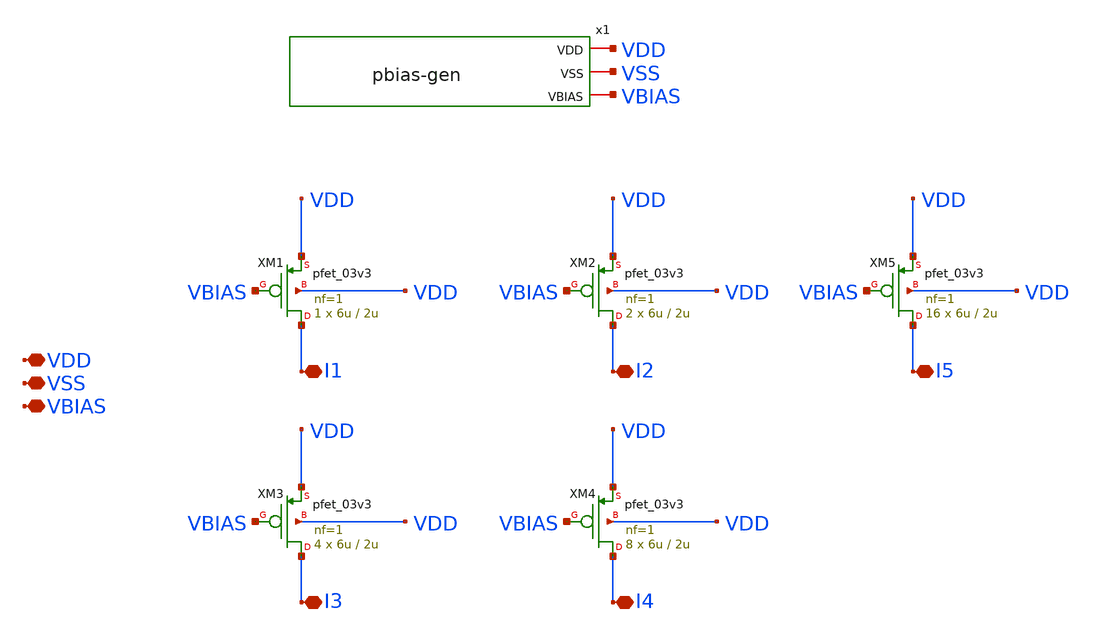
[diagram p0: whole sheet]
** sch_path: designs/libs/OTA/pmos_current_mirror-lna.sch
**.subckt pmos_current_mirror-lna VDD VSS VBIAS I1 I2 I3 I4 I5
*.iopin VDD
*.iopin VSS
*.iopin VBIAS
*.iopin I1
*.iopin I2
*.iopin I3
*.iopin I4
*.iopin I5
x1 VDD VSS VBIAS pbias-gen
XM1 I1 VBIAS VDD VDD pfet_03v3 L=2u W=6u nf=1 ad='int((nf+1)/2) * W/nf * 0.18u' as='int((nf+2)/2) * W/nf * 0.18u'
+ pd='2*int((nf+1)/2) * (W/nf + 0.18u)' ps='2*int((nf+2)/2) * (W/nf + 0.18u)' nrd='0.18u / W' nrs='0.18u / W'
+ sa=0 sb=0 sd=0 m=1
XM2 I2 VBIAS VDD VDD pfet_03v3 L=2u W=6u nf=1 ad='int((nf+1)/2) * W/nf * 0.18u' as='int((nf+2)/2) * W/nf * 0.18u'
+ pd='2*int((nf+1)/2) * (W/nf + 0.18u)' ps='2*int((nf+2)/2) * (W/nf + 0.18u)' nrd='0.18u / W' nrs='0.18u / W'
+ sa=0 sb=0 sd=0 m=2
XM3 I3 VBIAS VDD VDD pfet_03v3 L=2u W=6u nf=1 ad='int((nf+1)/2) * W/nf * 0.18u' as='int((nf+2)/2) * W/nf * 0.18u'
+ pd='2*int((nf+1)/2) * (W/nf + 0.18u)' ps='2*int((nf+2)/2) * (W/nf + 0.18u)' nrd='0.18u / W' nrs='0.18u / W'
+ sa=0 sb=0 sd=0 m=4
XM4 I4 VBIAS VDD VDD pfet_03v3 L=2u W=6u nf=1 ad='int((nf+1)/2) * W/nf * 0.18u' as='int((nf+2)/2) * W/nf * 0.18u'
+ pd='2*int((nf+1)/2) * (W/nf + 0.18u)' ps='2*int((nf+2)/2) * (W/nf + 0.18u)' nrd='0.18u / W' nrs='0.18u / W'
+ sa=0 sb=0 sd=0 m=8
XM5 I5 VBIAS VDD VDD pfet_03v3 L=2u W=6u nf=1 ad='int((nf+1)/2) * W/nf * 0.18u' as='int((nf+2)/2) * W/nf * 0.18u'
+ pd='2*int((nf+1)/2) * (W/nf + 0.18u)' ps='2*int((nf+2)/2) * (W/nf + 0.18u)' nrd='0.18u / W' nrs='0.18u / W'
+ sa=0 sb=0 sd=0 m=16
**.ends

* expanding   symbol:  libs/core_current-mirror/pbias-gen/pbias-gen.sym # of pins=3
** sym_path: designs/pbias-gen.sym
** sch_path: designs/pbias-gen.sch
.subckt pbias-gen VDD VSS VBIAS
*.iopin VDD
*.iopin VSS
*.iopin VBIAS
XR1 VSS VBIAS VSS ppolyf_u_3k r_width=0.25e-6 r_length=13.75e-6 m=1
XM1 VBIAS VBIAS VDD VDD pfet_03v3 L=5u W=15.5u nf=1 ad='int((nf+1)/2) * W/nf * 0.18u' as='int((nf+2)/2) * W/nf * 0.18u'
+ pd='2*int((nf+1)/2) * (W/nf + 0.18u)' ps='2*int((nf+2)/2) * (W/nf + 0.18u)' nrd='0.18u / W' nrs='0.18u / W'
+ sa=0 sb=0 sd=0 m=1
.ends

.end
